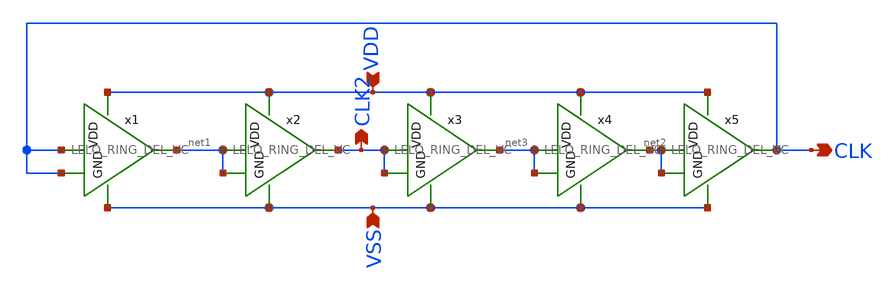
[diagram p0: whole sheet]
** sch_path: design/LELO_SVOD_SKY130A/RO.sch
**.subckt RO CLK VDD VSS CLK2
*.opin CLK
*.ipin VDD
*.ipin VSS
*.opin CLK2
x1 VDD CLK net1 VSS CLK LELO_RING_DEL_VC
x2 VDD net1 CLK2 VSS net1 LELO_RING_DEL_VC
x3 VDD CLK2 net3 VSS CLK2 LELO_RING_DEL_VC
x4 VDD net3 net2 VSS net3 LELO_RING_DEL_VC
x5 VDD net2 CLK VSS net2 LELO_RING_DEL_VC
**.ends

* expanding   symbol:  LELO_SVOD_SKY130A/LELO_RING_DEL_VC.sym # of pins=5
** sym_path: design/LELO_SVOD_SKY130A/LELO_RING_DEL_VC.sym
** sch_path: design/LELO_SVOD_SKY130A/LELO_RING_DEL_VC.sch
.subckt LELO_RING_DEL_VC VDD VIN VOUT GND VC
*.ipin VIN
*.ipin VDD
*.ipin GND
*.opin VOUT
*.ipin VC
XM1 VOUT VIN net1 GND sky130_fd_pr__nfet_01v8_lvt L=20 W=0.42 nf=1 ad='int((1 + 1)/2) * 0.42 / 1 * 0.29'
+ as='int((1 + 2)/2) * 0.42 / 1 * 0.29' pd='2*int((1 + 1)/2) * (0.42 / 1 + 0.29)' ps='2*int((1 + 2)/2) * (0.42 / 1 + 0.29)'
+ nrd='0.29 / 0.42 ' nrs='0.29 / 0.42 ' sa=0 sb=0 sd=0 mult=1 m=1
XM2 VOUT VIN net2 VDD sky130_fd_pr__pfet_01v8_lvt L=10 W=0.42 nf=1 ad='int((1 + 1)/2) * 0.42 / 1 * 0.29'
+ as='int((1 + 2)/2) * 0.42 / 1 * 0.29' pd='2*int((1 + 1)/2) * (0.42 / 1 + 0.29)' ps='2*int((1 + 2)/2) * (0.42 / 1 + 0.29)'
+ nrd='0.29 / 0.42 ' nrs='0.29 / 0.42 ' sa=0 sb=0 sd=0 mult=1 m=1
XM4 net1 VC GND GND sky130_fd_pr__nfet_01v8_lvt L=15 W=0.42 nf=1 ad='int((1 + 1)/2) * 0.42 / 1 * 0.29'
+ as='int((1 + 2)/2) * 0.42 / 1 * 0.29' pd='2*int((1 + 1)/2) * (0.42 / 1 + 0.29)' ps='2*int((1 + 2)/2) * (0.42 / 1 + 0.29)'
+ nrd='0.29 / 0.42 ' nrs='0.29 / 0.42 ' sa=0 sb=0 sd=0 mult=1 m=1
XM3 net2 VIN VDD VDD sky130_fd_pr__pfet_01v8_lvt L=10 W=0.42 nf=1 ad='int((1 + 1)/2) * 0.42 / 1 * 0.29'
+ as='int((1 + 2)/2) * 0.42 / 1 * 0.29' pd='2*int((1 + 1)/2) * (0.42 / 1 + 0.29)' ps='2*int((1 + 2)/2) * (0.42 / 1 + 0.29)'
+ nrd='0.29 / 0.42 ' nrs='0.29 / 0.42 ' sa=0 sb=0 sd=0 mult=1 m=1
.ends

.end
